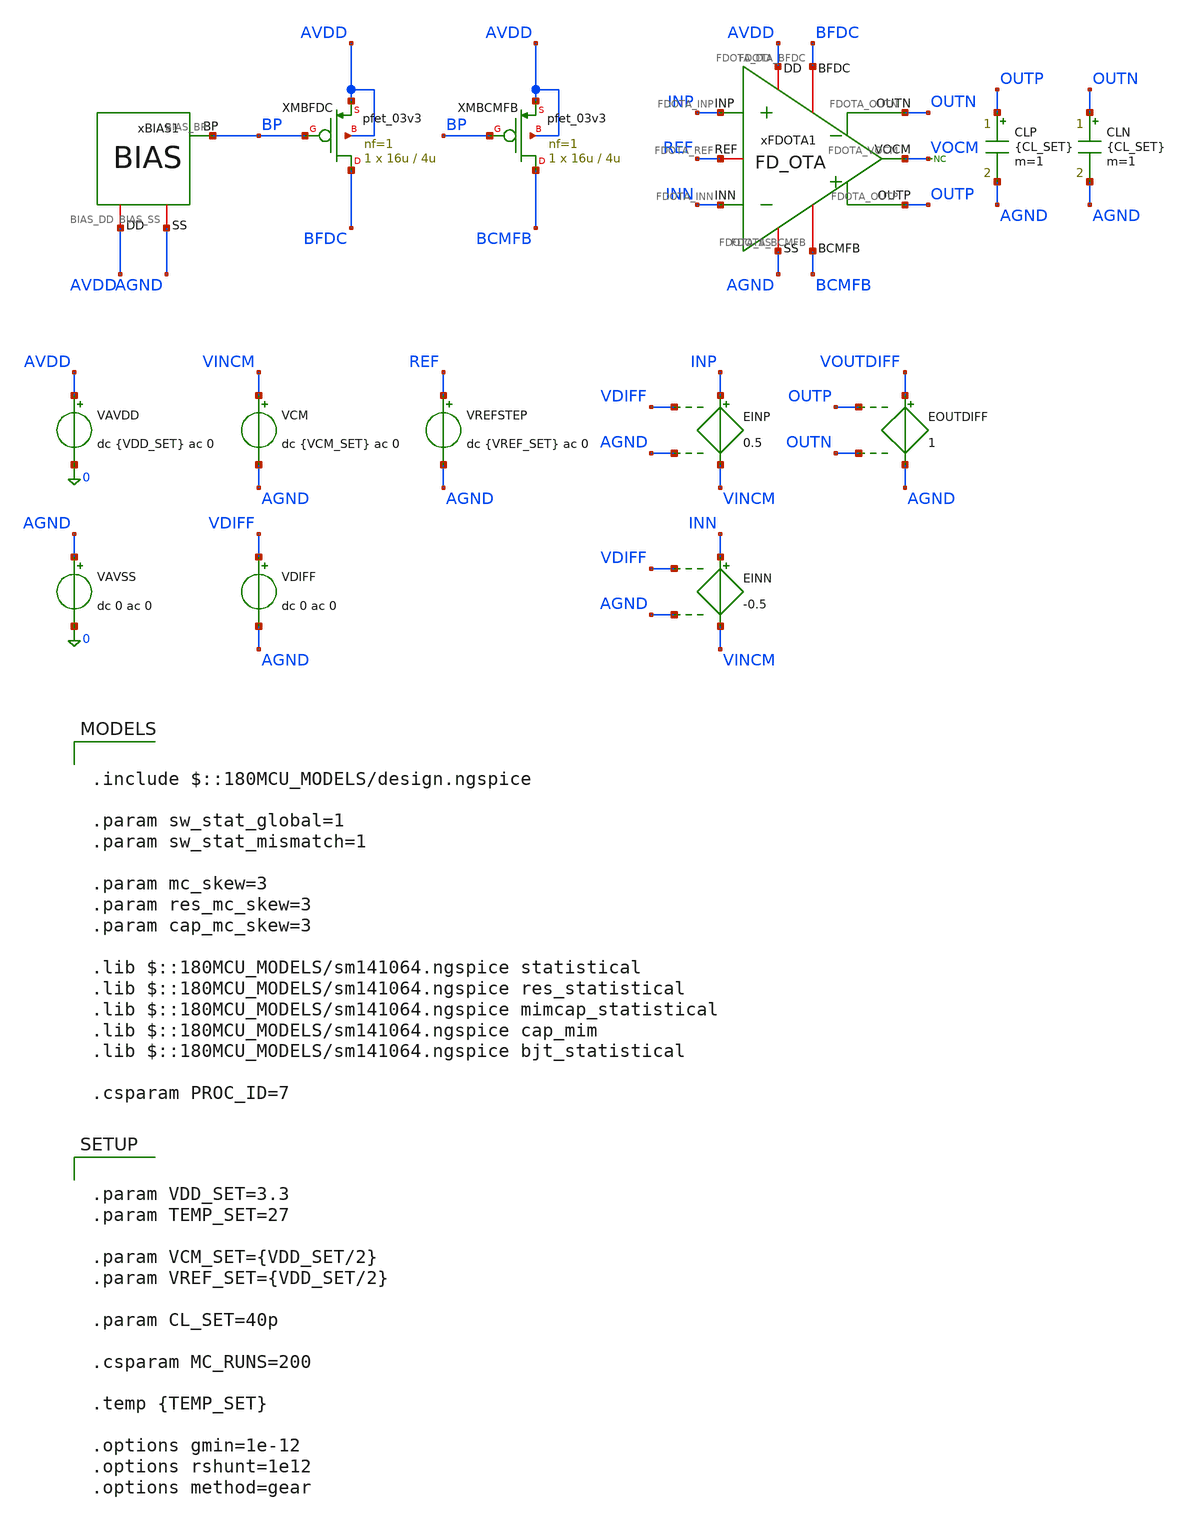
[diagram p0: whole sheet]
** sch_path: Design_Files/IC Design/Testbench/ANALOG_BLOCKS/FD_OTA/Open_Loop/FD_OTA_TB_OL_FULL.sch
**.subckt FD_OTA_TB_OL_FULL
VAVDD AVDD 0 dc {VDD_SET} ac 0
.save i(vavdd)
VCM VINCM AGND dc {VCM_SET} ac 0
VDIFF VDIFF AGND dc 0 ac 0
VAVSS AGND 0 dc 0 ac 0
EINP INP VINCM VDIFF AGND 0.5
EINN INN VINCM VDIFF AGND -0.5
CLP OUTP AGND {CL_SET} m=1
CLN OUTN AGND {CL_SET} m=1
* noconn VOCM
xFDOTA1 AVDD AGND INP INN OUTN BFDC OUTP BCMFB REF VOCM FD_OTA
xBIAS1 AVDD AGND BP BIAS
XMBFDC BFDC BP AVDD AVDD pfet_03v3 L=4u W=16u nf=1 ad='int((nf+1)/2) * W/nf * 0.18u' as='int((nf+2)/2) * W/nf * 0.18u'
+ pd='2*int((nf+1)/2) * (W/nf + 0.18u)' ps='2*int((nf+2)/2) * (W/nf + 0.18u)' nrd='0.18u / W' nrs='0.18u / W'
+ sa=0 sb=0 sd=0 m=1
XMBCMFB BCMFB BP AVDD AVDD pfet_03v3 L=4u W=16u nf=1 ad='int((nf+1)/2) * W/nf * 0.18u' as='int((nf+2)/2) * W/nf * 0.18u'
+ pd='2*int((nf+1)/2) * (W/nf + 0.18u)' ps='2*int((nf+2)/2) * (W/nf + 0.18u)' nrd='0.18u / W' nrs='0.18u / W'
+ sa=0 sb=0 sd=0 m=1
EOUTDIFF VOUTDIFF AGND OUTP OUTN 1
VREFSTEP REF AGND dc {VREF_SET} ac 0
**** begin user architecture code

.include $::180MCU_MODELS/design.ngspice

.param sw_stat_global=1
.param sw_stat_mismatch=1

.param mc_skew=3
.param res_mc_skew=3
.param cap_mc_skew=3

.lib $::180MCU_MODELS/sm141064.ngspice statistical
.lib $::180MCU_MODELS/sm141064.ngspice res_statistical
.lib $::180MCU_MODELS/sm141064.ngspice mimcap_statistical
.lib $::180MCU_MODELS/sm141064.ngspice cap_mim
.lib $::180MCU_MODELS/sm141064.ngspice bjt_statistical

.csparam PROC_ID=7




.control

destroy all

set noaskquit
set wr_singlescale
unset wr_vecnames

option klu
option numdgt=15
option method=gear
option maxord=2
option plotwinsize=0
option rshunt=1e12


if $&PROC_ID = 5
set proc=MM
else
if $&PROC_ID = 6
set proc=GL
else
set proc=FULL
end
end


shell mkdir -p /foss/designs/ECG_Acquisition_IC/Measurement_Results/IC_Simulation/ANALOG_BLOCKS/FD_OTA/{$proc}.Result_txt

shell rm -f /foss/designs/ECG_Acquisition_IC/Measurement_Results/IC_Simulation/ANALOG_BLOCKS/FD_OTA/{$proc}.Result_txt/{$proc}.ol_mc_summary.txt
shell rm -f /foss/designs/ECG_Acquisition_IC/Measurement_Results/IC_Simulation/ANALOG_BLOCKS/FD_OTA/{$proc}.Result_txt/{$proc}.ol_mc_debug_op.txt


echo run vos_V dc_gain_dB ugf_Hz phase_ugf_deg pm_deg > /foss/designs/ECG_Acquisition_IC/Measurement_Results/IC_Simulation/ANALOG_BLOCKS/FD_OTA/{$proc}.Result_txt/{$proc}.ol_mc_summary.txt

echo run vos_V outp_zero_V outn_zero_V outdiff_zero_V outp_center_V outn_center_V outcm_center_V outdiff_center_V
+ ref_V vocm_V > /foss/designs/ECG_Acquisition_IC/Measurement_Results/IC_Simulation/ANALOG_BLOCKS/FD_OTA/{$proc}.Result_txt/{$proc}.ol_mc_debug_op.txt


let run=1
let mc_runs=$&MC_RUNS


dowhile run <= mc_runs

set runnum=$&run

setseed $runnum
mc_source


option klu
option numdgt=15
option method=gear
option maxord=2
option plotwinsize=0
option rshunt=1e12


* SOURCES

alter @VAVDD[DC]=3.3
alter @VAVSS[DC]=0

alter @VCM[DC]=1.65
alter @VDIFF[DC]=0
alter @VREFSTEP[DC]=1.65

alter @VAVDD[ACMAG]=0
alter @VAVSS[ACMAG]=0
alter @VCM[ACMAG]=0
alter @VDIFF[ACMAG]=0
alter @VREFSTEP[ACMAG]=0


* OFFSET + ZERO INPUT VALUES

save INP INN OUTP OUTN REF VOCM

dc VDIFF -10m 10m 10u

let outdiff_sweep=v(OUTP)-v(OUTN)

meas dc outp_zero_meas find v(OUTP) at=0
meas dc outn_zero_meas find v(OUTN) at=0
meas dc outdiff_zero_meas find outdiff_sweep at=0

meas dc vos_center when outdiff_sweep=0 cross=1

set outp_zero_val=$&outp_zero_meas
set outn_zero_val=$&outn_zero_meas
set outdiff_zero_val=$&outdiff_zero_meas
set vos_val=$&vos_center

destroy all


* CENTER OP

alter @VDIFF[DC]=$vos_val

save OUTP OUTN REF VOCM

op

let outp_center=v(OUTP)-v(AGND)
let outn_center=v(OUTN)-v(AGND)

let outcm_center=0.5*(outp_center+outn_center)
let outdiff_center=outp_center-outn_center

let ref_center=v(REF)-v(AGND)
let vocm_center=v(VOCM)-v(AGND)

set outp_center_val=$&outp_center
set outn_center_val=$&outn_center
set outcm_center_val=$&outcm_center
set outdiff_center_val=$&outdiff_center
set ref_val=$&ref_center
set vocm_val=$&vocm_center


echo $runnum $vos_val $outp_zero_val $outn_zero_val $outdiff_zero_val $outp_center_val $outn_center_val
+ $outcm_center_val $outdiff_center_val $ref_val $vocm_val >> /foss/designs/ECG_Acquisition_IC/Measurement_Results/IC_Simulation/ANALOG_BLOCKS/FD_OTA/{$proc}.Result_txt/{$proc}.ol_mc_debug_op.txt

destroy all


* DIFFERENTIAL AC

alter @VDIFF[DC]=$vos_val

alter @VCM[ACMAG]=0

alter @VDIFF[ACMAG]=1
alter @VDIFF[ACPHASE]=0

alter @VREFSTEP[ACMAG]=0
alter @VAVDD[ACMAG]=0
alter @VAVSS[ACMAG]=0

save INP INN OUTP OUTN

ac dec 100 1 200Meg

let vin_diff=v(INP)-v(INN)
let vout_diff=v(OUTP)-v(OUTN)

let ol_tf=vout_diff/vin_diff

let ol_gain=mag(ol_tf)
let ol_gain_db=db(ol_tf)
let ol_phase=(180/3.141592653589793)*cph(ol_tf)

meas ac dc_gain_db find ol_gain_db at=1

meas ac ugf_meas when ol_gain=1 fall=1

meas ac phase_ugf find ol_phase at=$&ugf_meas

let pm_calc=180+phase_ugf

set gain_db_val=$&dc_gain_db
set ugf_val=$&ugf_meas
set phase_val=$&phase_ugf
set pm_val=$&pm_calc


echo $runnum $vos_val $gain_db_val $ugf_val $phase_val $pm_val >> /foss/designs/ECG_Acquisition_IC/Measurement_Results/IC_Simulation/ANALOG_BLOCKS/FD_OTA/{$proc}.Result_txt/{$proc}.ol_mc_summary.txt


destroy all

let run=run+1

end


quit

.endc




.param VDD_SET=3.3
.param TEMP_SET=27

.param VCM_SET={VDD_SET/2}
.param VREF_SET={VDD_SET/2}

.param CL_SET=40p

.csparam MC_RUNS=200

.temp {TEMP_SET}

.options gmin=1e-12
.options rshunt=1e12
.options method=gear


**** end user architecture code
**.ends
.end
